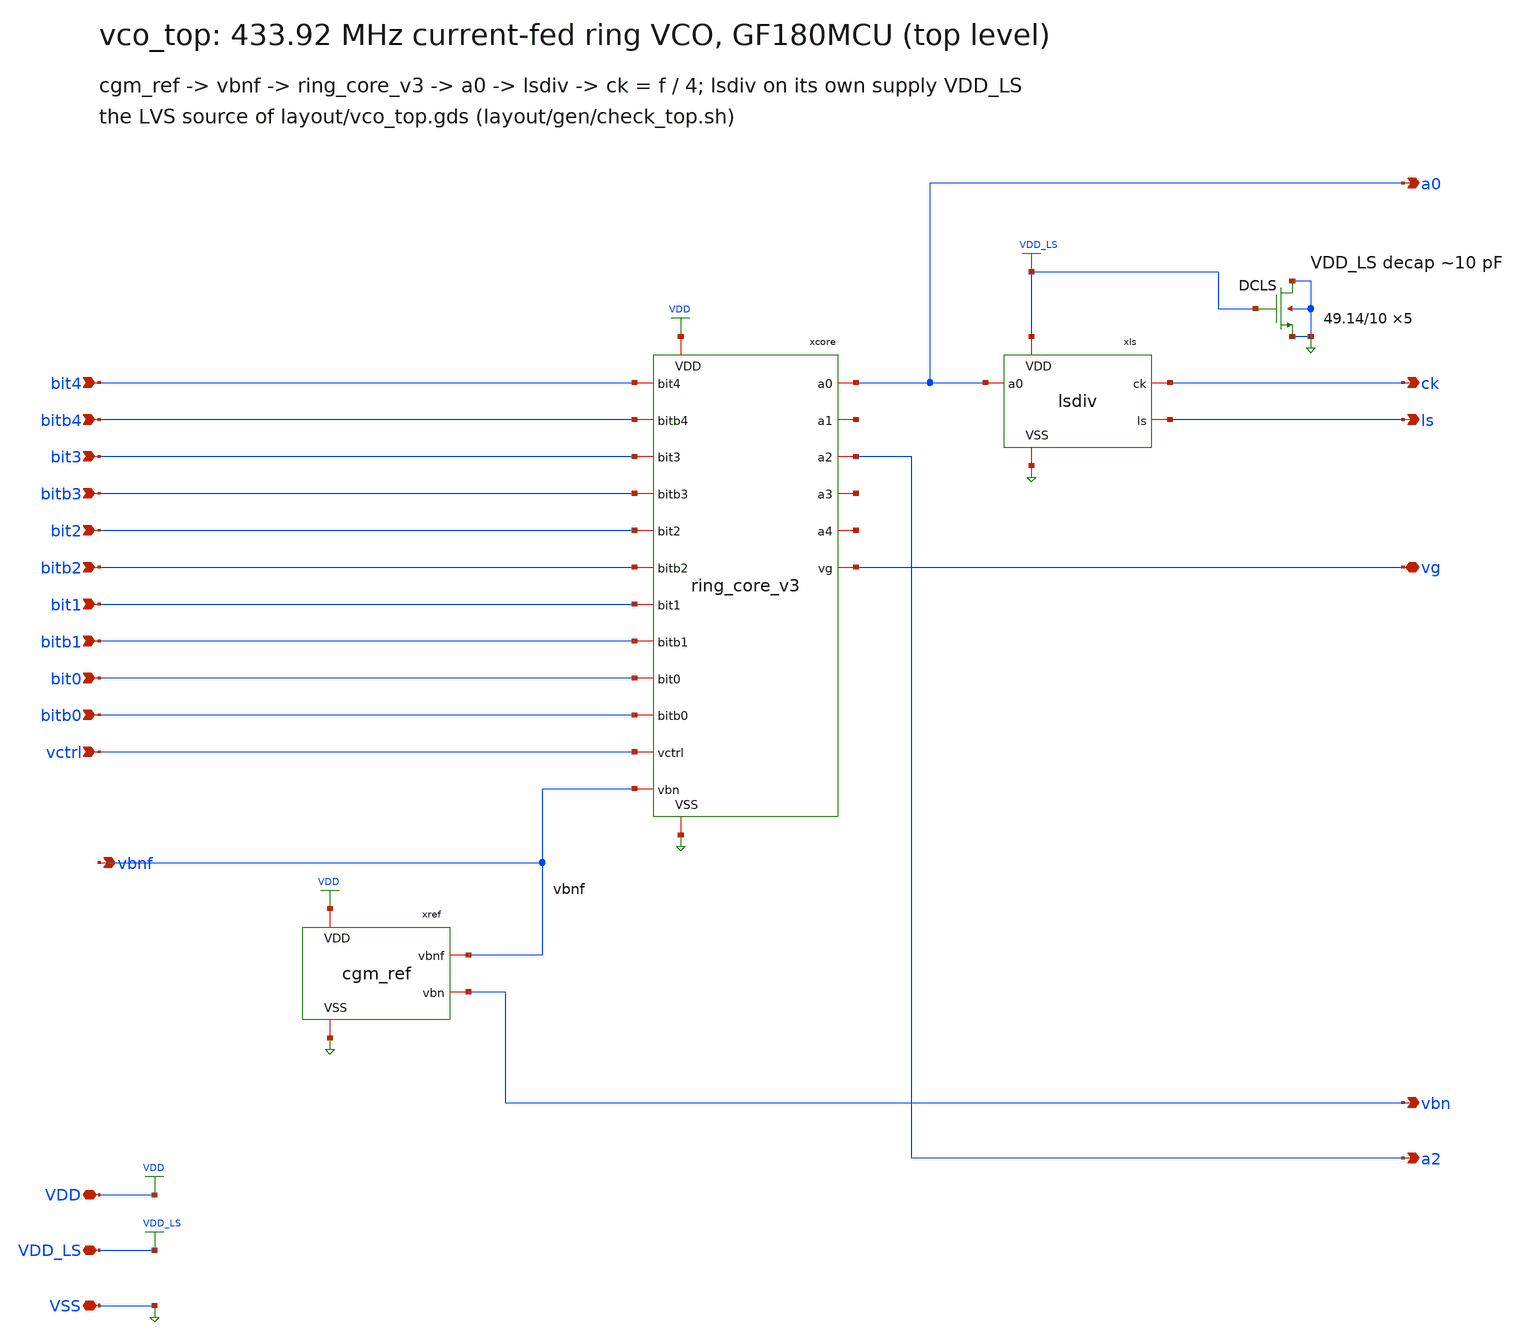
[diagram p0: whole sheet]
** sch_path: xschem/vco_top.sch
**.subckt vco_top VDD VDD_LS VSS vctrl bit0 bit1 bit2 bit3 bit4 bitb0 bitb1 bitb2 bitb3 bitb4 ck a0
*+ vbn vg ls vbnf a2
*.iopin VDD
*.iopin VDD_LS
*.iopin VSS
*.ipin vctrl
*.ipin bit0
*.ipin bit1
*.ipin bit2
*.ipin bit3
*.ipin bit4
*.ipin bitb0
*.ipin bitb1
*.ipin bitb2
*.ipin bitb3
*.ipin bitb4
*.opin ck
*.opin a0
*.opin vbn
*.iopin vg
*.opin ls
*.opin vbnf
*.opin a2
xcore VDD VSS vbnf vctrl bit0 bit1 bit2 bit3 bit4 bitb0 bitb1 bitb2 bitb3 bitb4 vg a0 net1 a2 net2
+ net3 ring_core_v3
xref VDD VSS vbn vbnf cgm_ref
xls VDD_LS VSS a0 ck ls lsdiv
XDCLS VSS VDD_LS VSS VSS nfet_03v3 L=10.0u W=49.14u nf=1 ad=0 as=0 pd=0 ps=0 nrd=0 nrs=0 sa=0 sb=0
+ sd=0 m=5
**.ends
.end
